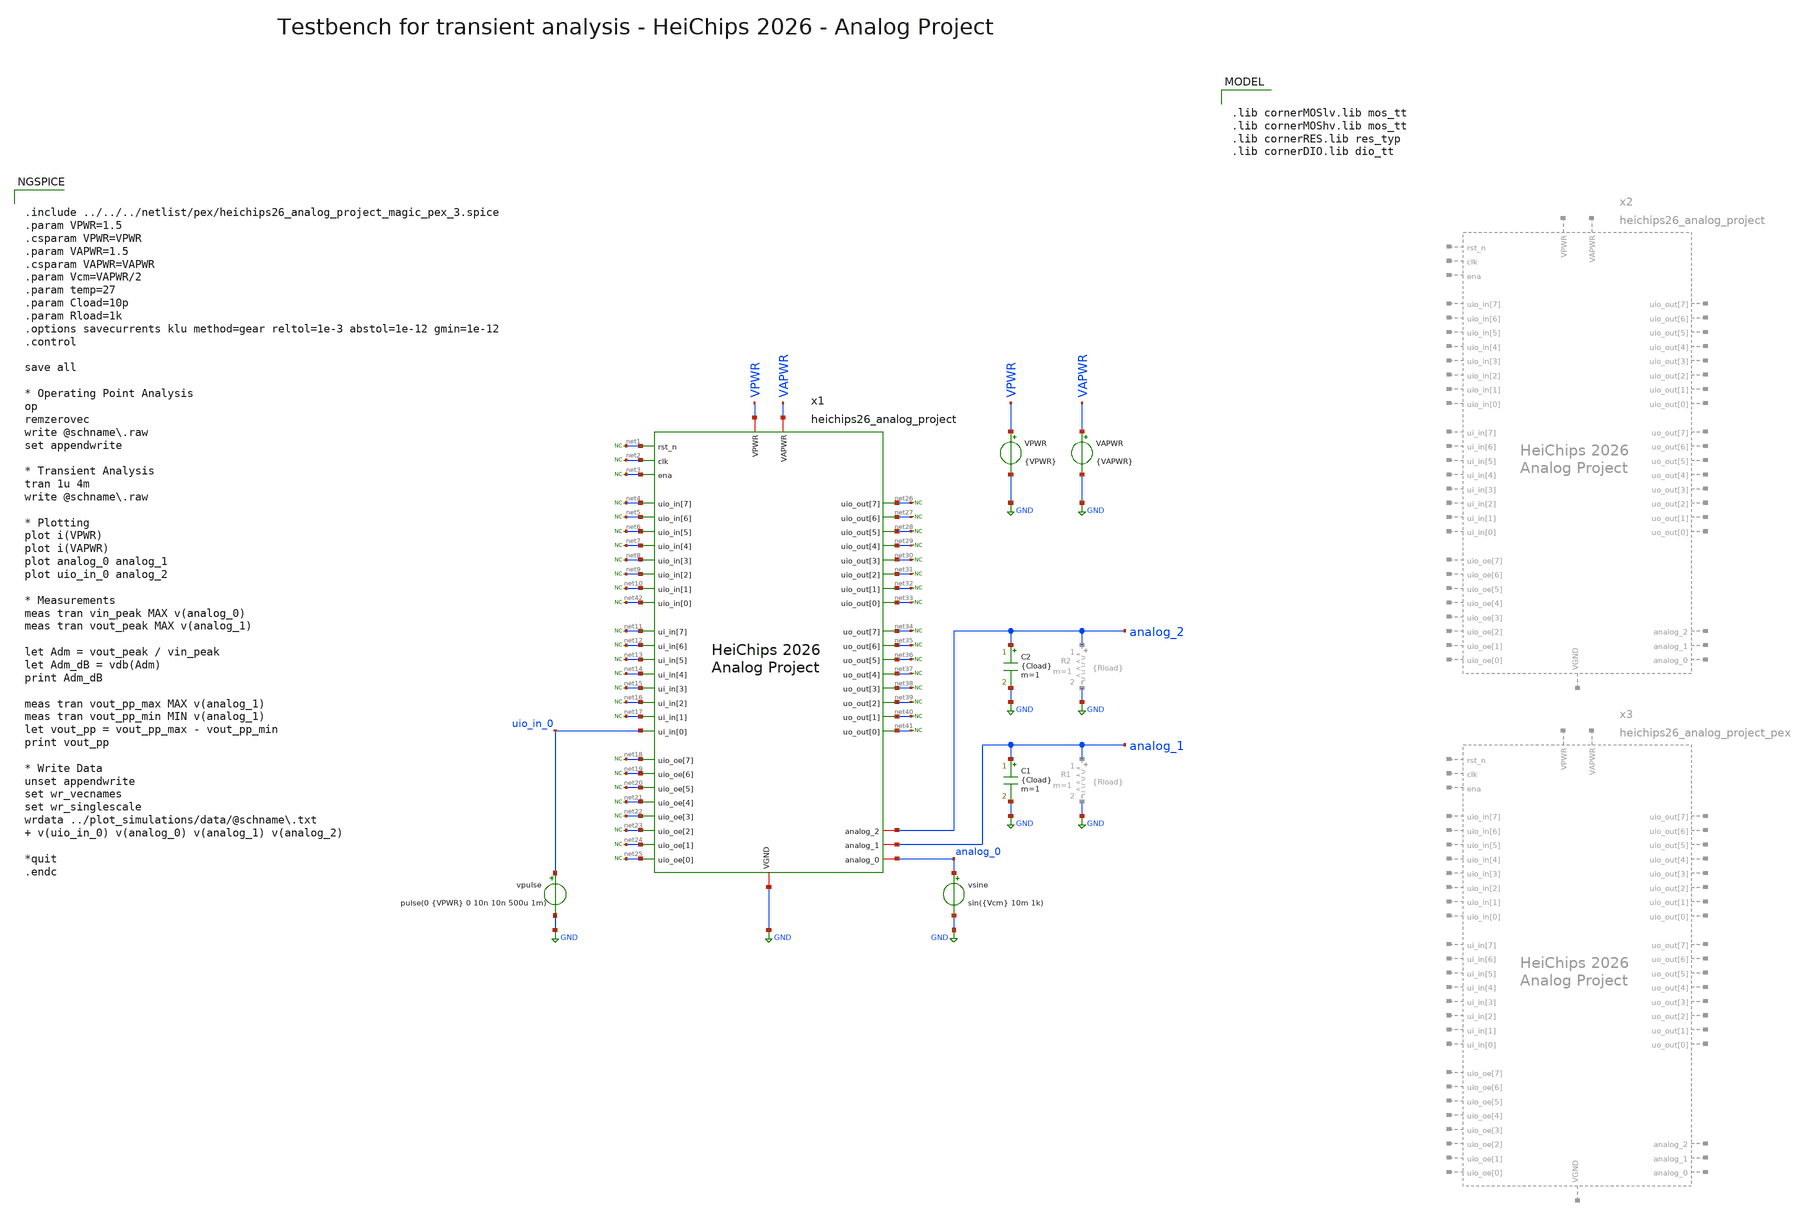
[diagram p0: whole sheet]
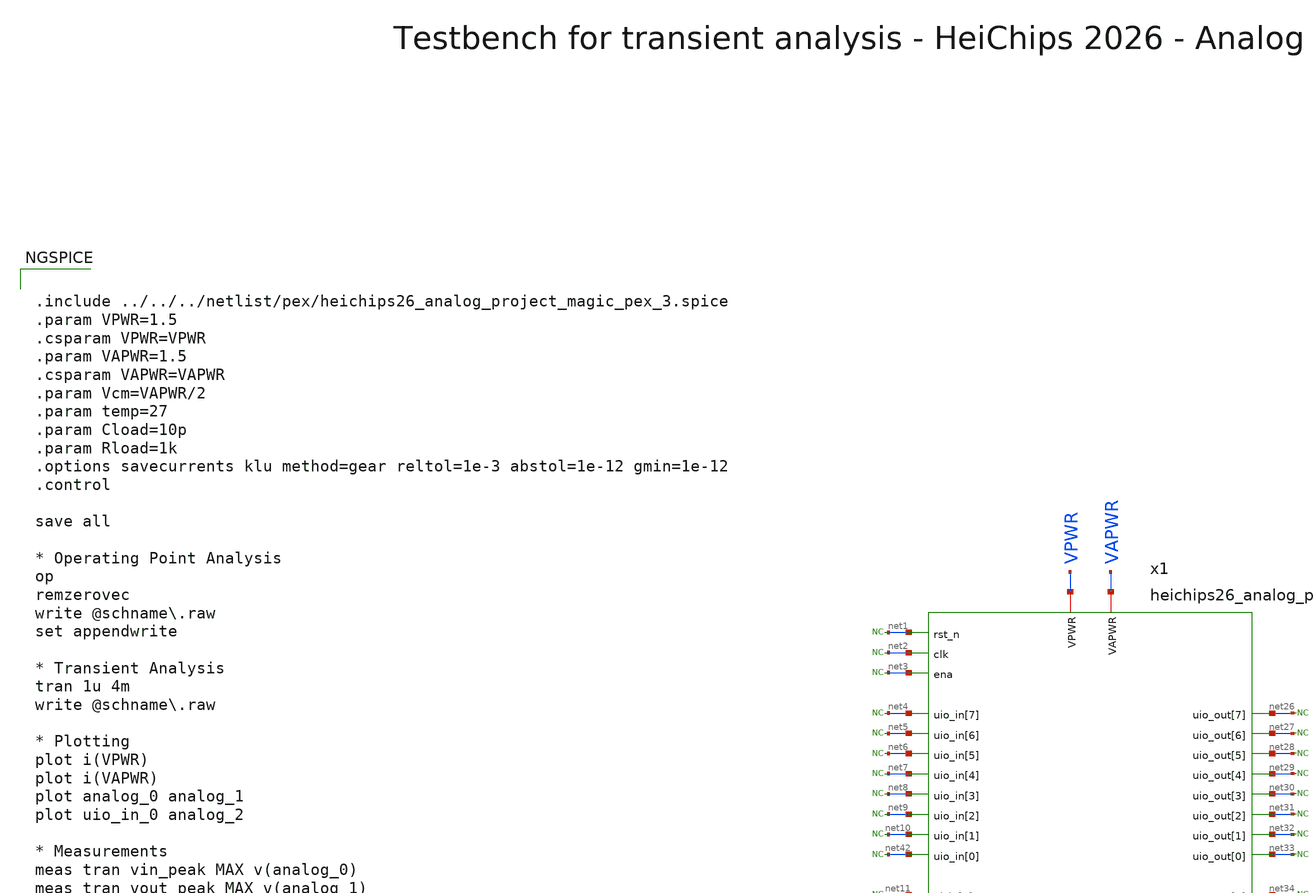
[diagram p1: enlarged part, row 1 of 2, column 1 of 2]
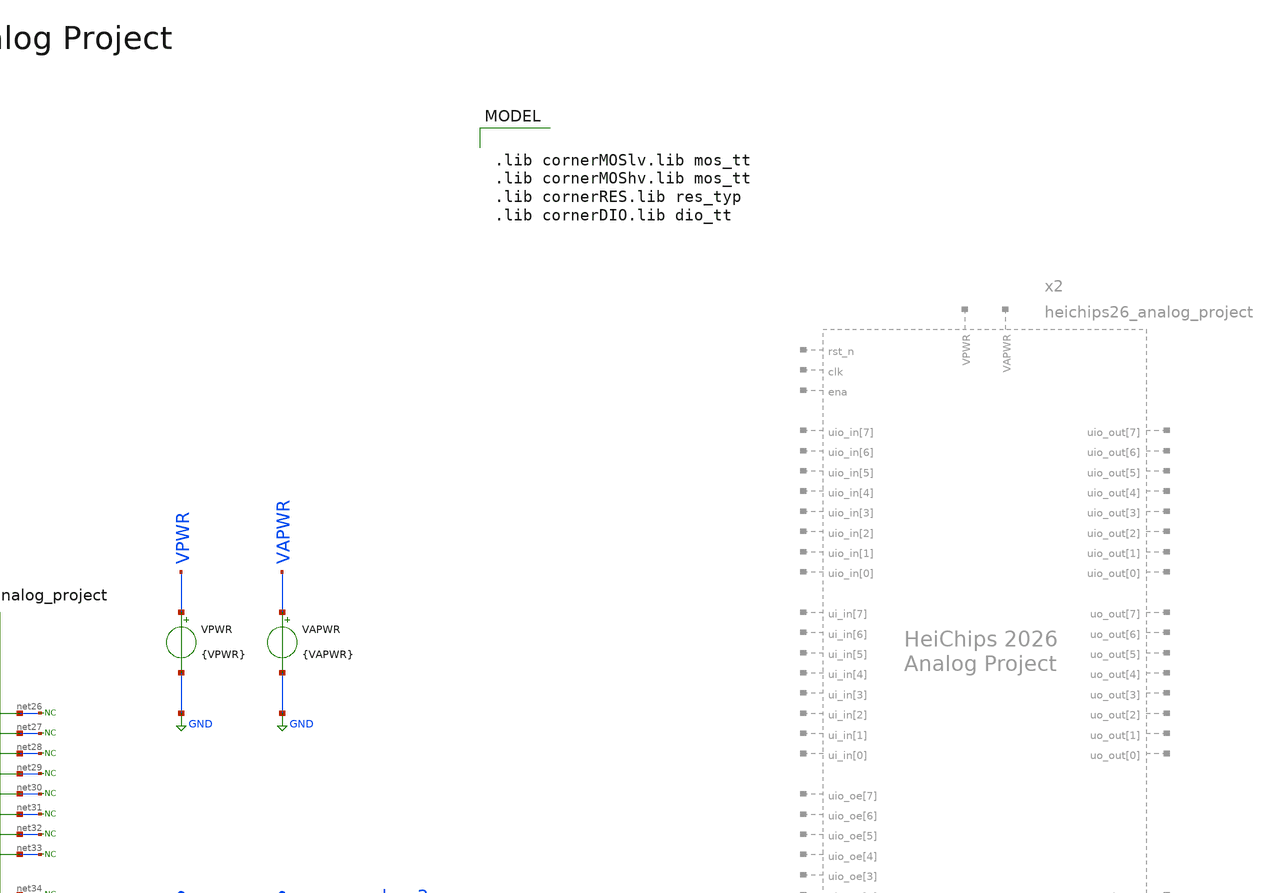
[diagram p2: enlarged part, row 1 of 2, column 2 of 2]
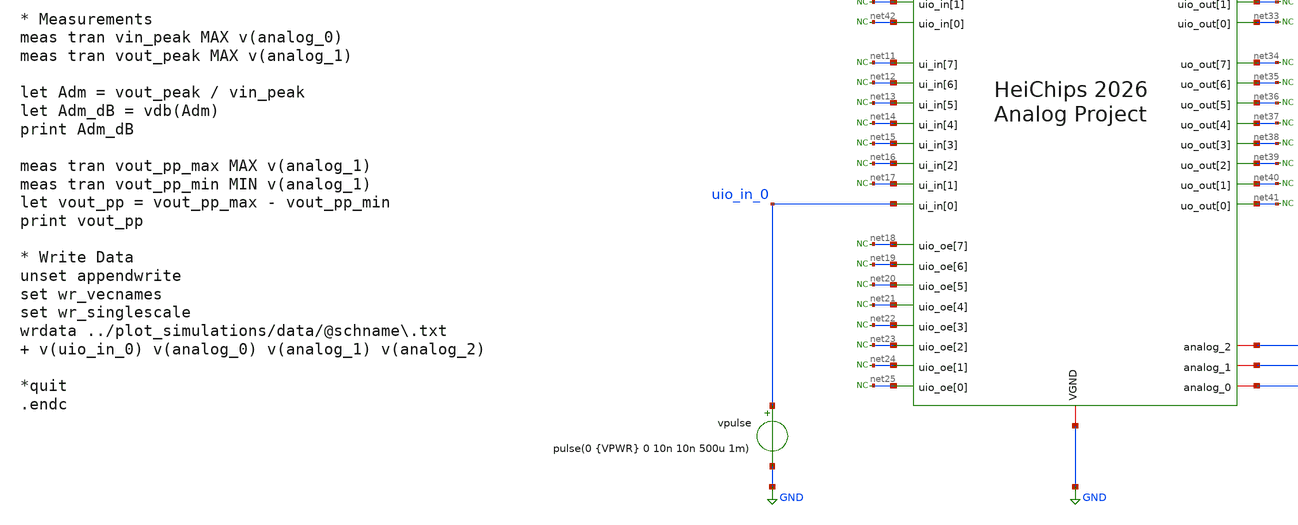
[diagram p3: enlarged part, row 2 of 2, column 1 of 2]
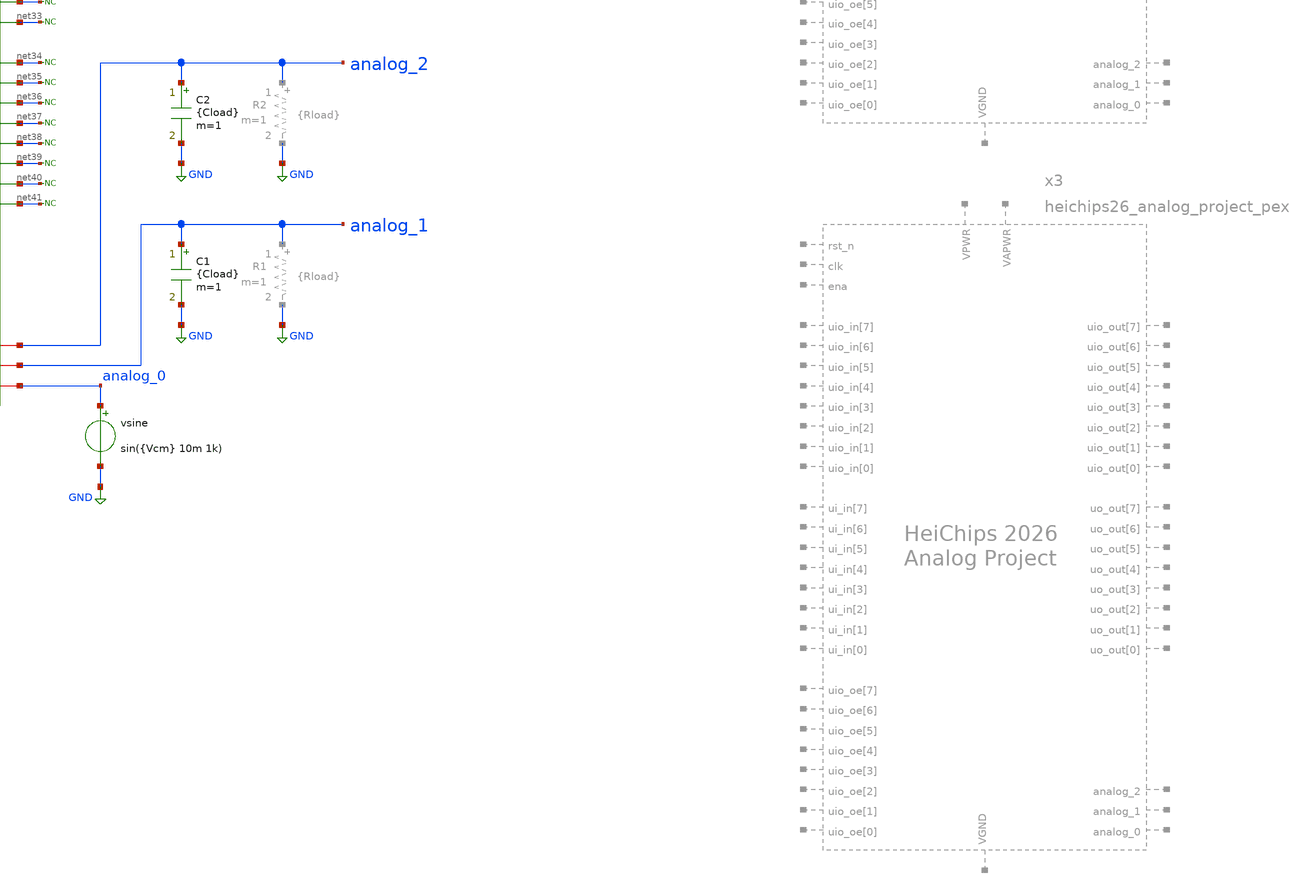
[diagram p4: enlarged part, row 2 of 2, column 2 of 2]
** sch_path: macros/heichips26_analog_project/testbenches/xschem/heichips26_analog_project_tb_tran.sch
**.subckt heichips26_analog_project_tb_tran
VPWR VPWR GND {VPWR}
vsine analog_0 GND sin({Vcm} 10m 1k)
C1 analog_1 GND {Cload} m=1
C2 analog_2 GND {Cload} m=1
* noconn #net26
* noconn #net27
* noconn #net28
* noconn #net29
* noconn #net30
* noconn #net31
* noconn #net32
* noconn #net33
* noconn #net34
* noconn #net35
* noconn #net36
* noconn #net37
* noconn #net38
* noconn #net39
* noconn #net40
* noconn #net41
* noconn #net1
* noconn #net2
* noconn #net3
* noconn #net4
* noconn #net5
* noconn #net6
* noconn #net7
* noconn #net8
* noconn #net9
* noconn #net10
* noconn #net11
* noconn #net12
* noconn #net13
* noconn #net14
* noconn #net15
* noconn #net16
* noconn #net17
* noconn #net18
* noconn #net19
* noconn #net20
* noconn #net21
* noconn #net22
* noconn #net23
* noconn #net24
* noconn #net25
VAPWR VAPWR GND {VAPWR}
vpulse uio_in_0 GND pulse(0 {VPWR} 0 10n 10n 500u 1m)
* noconn #net42
x1 VPWR VAPWR GND net1 net2 net3 net4 net5 net6 net7 net8 net9 net10 net42 net11 net12 net13 net14
+ net15 net16 net17 uio_in_0 net18 net19 net20 net21 net22 net23 net24 net25 net26 net27 net28 net29 net30
+ net31 net32 net33 net34 net35 net36 net37 net38 net39 net40 net41 analog_2 analog_1 analog_0
+ heichips26_analog_project
**** begin user architecture code


.include ../../../netlist/pex/heichips26_analog_project_magic_pex_3.spice
.param VPWR=1.5
.csparam VPWR=VPWR
.param VAPWR=1.5
.csparam VAPWR=VAPWR
.param Vcm=VAPWR/2
.param temp=27
.param Cload=10p
.param Rload=1k
.options savecurrents klu method=gear reltol=1e-3 abstol=1e-12 gmin=1e-12
.control

save all

* Operating Point Analysis
op
remzerovec
write @schname\.raw
set appendwrite

* Transient Analysis
tran 1u 4m
write @schname\.raw

* Plotting
plot i(VPWR)
plot i(VAPWR)
plot analog_0 analog_1
plot uio_in_0 analog_2

* Measurements
meas tran vin_peak MAX v(analog_0)
meas tran vout_peak MAX v(analog_1)

let Adm = vout_peak / vin_peak
let Adm_dB = vdb(Adm)
print Adm_dB

meas tran vout_pp_max MAX v(analog_1)
meas tran vout_pp_min MIN v(analog_1)
let vout_pp = vout_pp_max - vout_pp_min
print vout_pp

* Write Data
unset appendwrite
set wr_vecnames
set wr_singlescale
wrdata ../plot_simulations/data/@schname\.txt  v(uio_in_0) v(analog_0) v(analog_1) v(analog_2)

*quit
.endc



.lib cornerMOSlv.lib mos_tt
.lib cornerMOShv.lib mos_tt
.lib cornerRES.lib res_typ
.lib cornerDIO.lib dio_tt

**** end user architecture code
**.ends
.GLOBAL GND
.end
